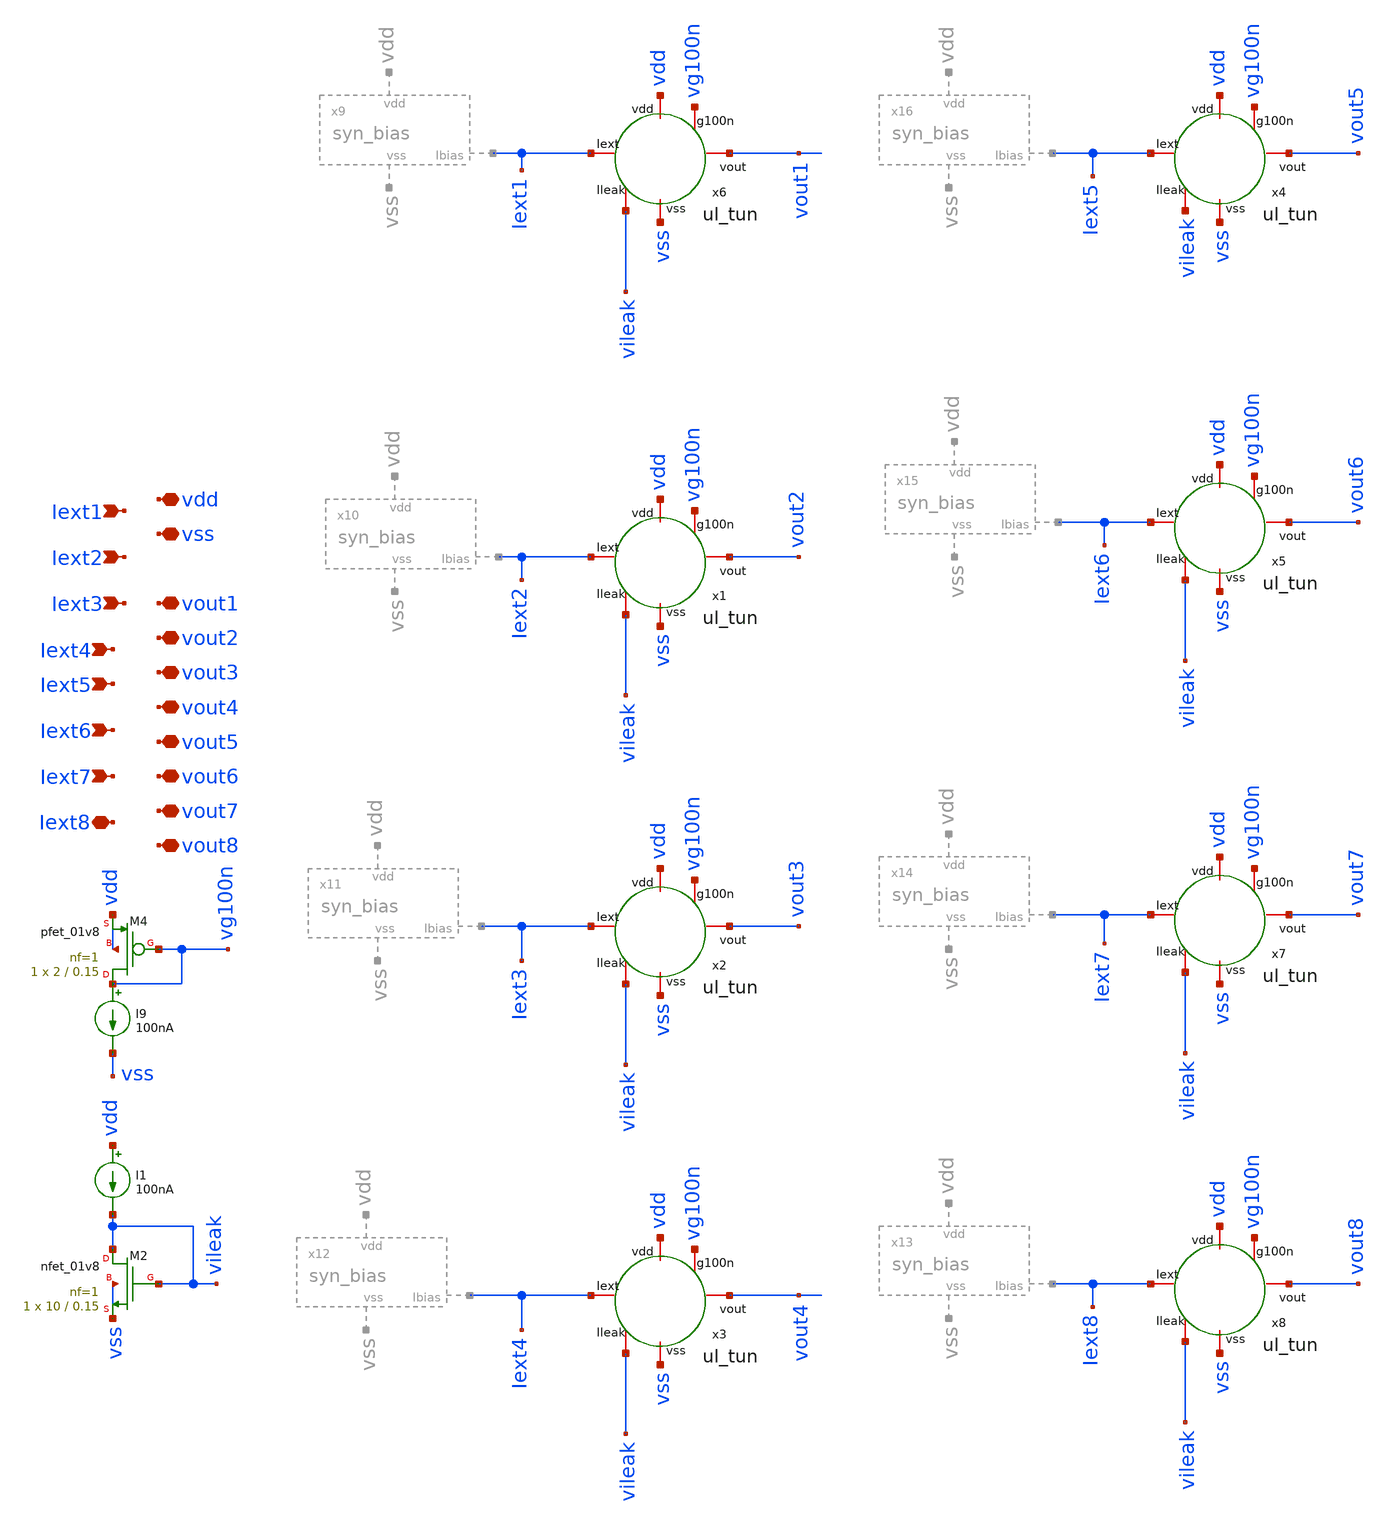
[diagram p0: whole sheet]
** sch_path: layer/layer_hidden.sch
**.subckt layer_hidden vdd vss Iext1 Iext2 Iext3 Iext4 vout1 vout2 vout3 vout4 Iext5 Iext6 Iext7
*+ Iext8 vout5 vout6 vout7 vout8
*.iopin vdd
*.iopin vss
*.ipin Iext1
*.ipin Iext2
*.ipin Iext3
*.ipin Iext4
*.iopin vout1
*.iopin vout2
*.iopin vout3
*.iopin vout4
*.ipin Iext5
*.ipin Iext6
*.ipin Iext7
*.iopin Iext8
*.iopin vout5
*.iopin vout6
*.iopin vout7
*.iopin vout8
x6 Iext1 vdd vg100n vout1 vileak vss ul_tun
I9 vg100n vss 100nA
XM4 vg100n vg100n vdd vdd sky130_fd_pr__pfet_01v8 L=0.15 W=2 nf=1 ad='int((nf+1)/2) * W/nf * 0.29' as='int((nf+2)/2) * W/nf * 0.29'
+ pd='2*int((nf+1)/2) * (W/nf + 0.29)' ps='2*int((nf+2)/2) * (W/nf + 0.29)' nrd='0.29 / W' nrs='0.29 / W'
+ sa=0 sb=0 sd=0 mult=1 m=1
XM2 vileak vileak vss vss sky130_fd_pr__nfet_01v8 L=0.15 W=10 nf=1 ad='int((nf+1)/2) * W/nf * 0.29' as='int((nf+2)/2) * W/nf * 0.29'
+ pd='2*int((nf+1)/2) * (W/nf + 0.29)' ps='2*int((nf+2)/2) * (W/nf + 0.29)' nrd='0.29 / W' nrs='0.29 / W'
+ sa=0 sb=0 sd=0 mult=1 m=1
I1 vdd vileak 100nA
x1 Iext2 vdd vg100n vout2 vileak vss ul_tun
x2 Iext3 vdd vg100n vout3 vileak vss ul_tun
x3 Iext4 vdd vg100n vout4 vileak vss ul_tun
x8 Iext8 vdd vg100n vout8 vileak vss ul_tun
x4 Iext5 vdd vg100n vout5 vileak vss ul_tun
x5 Iext6 vdd vg100n vout6 vileak vss ul_tun
x7 Iext7 vdd vg100n vout7 vileak vss ul_tun
**.ends

* expanding   symbol:  Neuron/ultralif/ul_tun.sym # of pins=6
** sym_path: Neuron/ultralif/ul_tun.sym
** sch_path: Neuron/ultralif/ul_tun.sch
.subckt ul_tun Iext vdd g100n vout Ileak vss
*.iopin Iext
*.iopin vout
*.iopin vss
*.iopin Ileak
*.iopin vdd
*.iopin g100n
XM1 Ileak Ileak net1 vdd sky130_fd_pr__pfet_01v8 L=10 W=1 nf=1 ad='int((nf+1)/2) * W/nf * 0.29' as='int((nf+2)/2) * W/nf * 0.29'
+ pd='2*int((nf+1)/2) * (W/nf + 0.29)' ps='2*int((nf+2)/2) * (W/nf + 0.29)' nrd='0.29 / W' nrs='0.29 / W'
+ sa=0 sb=0 sd=0 mult=1 m=1
XM2 Ileak net2 net1 vdd sky130_fd_pr__pfet_01v8 L=0.15 W=1.5 nf=1 ad='int((nf+1)/2) * W/nf * 0.29' as='int((nf+2)/2) * W/nf * 0.29'
+ pd='2*int((nf+1)/2) * (W/nf + 0.29)' ps='2*int((nf+2)/2) * (W/nf + 0.29)' nrd='0.29 / W' nrs='0.29 / W'
+ sa=0 sb=0 sd=0 mult=1 m=1
XM3 net2 net2 net1 vdd sky130_fd_pr__pfet_01v8 L=0.15 W=15 nf=1 ad='int((nf+1)/2) * W/nf * 0.29' as='int((nf+2)/2) * W/nf * 0.29'
+ pd='2*int((nf+1)/2) * (W/nf + 0.29)' ps='2*int((nf+2)/2) * (W/nf + 0.29)' nrd='0.29 / W' nrs='0.29 / W'
+ sa=0 sb=0 sd=0 mult=1 m=1
XM4 net2 Ileak vss vss sky130_fd_pr__nfet_01v8 L=4 W=1 nf=1 ad='int((1 + 1)/2) * 1 / 1 * 0.29' as='int((1 + 2)/2) * 1 / 1 * 0.29'
+ pd='2*int((1 + 1)/2) * (1 / 1 + 0.29)' ps='2*int((1 + 2)/2) * (1 / 1 + 0.29)' nrd='0.29 / 1 ' nrs='0.29 / 1 '
+ sa=0 sb=0 sd=0 mult=1 m=1
C1 net1 vss 1p m=1
XM5 vout_n Ileak vss vss sky130_fd_pr__nfet_01v8 L=0.15 W=1 nf=1 ad='int((1 + 1)/2) * 1 / 1 * 0.29' as='int((1 + 2)/2) * 1 / 1 * 0.29'
+ pd='2*int((1 + 1)/2) * (1 / 1 + 0.29)' ps='2*int((1 + 2)/2) * (1 / 1 + 0.29)' nrd='0.29 / 1 ' nrs='0.29 / 1 '
+ sa=0 sb=0 sd=0 mult=1 m=1
XM6 vout_n g100n vdd vdd sky130_fd_pr__pfet_01v8 L=0.15 W=2 nf=1 ad='int((nf+1)/2) * W/nf * 0.29' as='int((nf+2)/2) * W/nf * 0.29'
+ pd='2*int((nf+1)/2) * (W/nf + 0.29)' ps='2*int((nf+2)/2) * (W/nf + 0.29)' nrd='0.29 / W' nrs='0.29 / W'
+ sa=0 sb=0 sd=0 mult=1 m=1
XM7 vout vout_n vss vss sky130_fd_pr__nfet_01v8 L=0.15 W=1 nf=1 ad='int((1 + 1)/2) * 1 / 1 * 0.29' as='int((1 + 2)/2) * 1 / 1 * 0.29'
+ pd='2*int((1 + 1)/2) * (1 / 1 + 0.29)' ps='2*int((1 + 2)/2) * (1 / 1 + 0.29)' nrd='0.29 / 1 ' nrs='0.29 / 1 '
+ sa=0 sb=0 sd=0 mult=1 m=1
XM8 vout vout_n vdd vdd sky130_fd_pr__pfet_01v8 L=0.15 W=2 nf=1 ad='int((nf+1)/2) * W/nf * 0.29' as='int((nf+2)/2) * W/nf * 0.29'
+ pd='2*int((nf+1)/2) * (W/nf + 0.29)' ps='2*int((nf+2)/2) * (W/nf + 0.29)' nrd='0.29 / W' nrs='0.29 / W'
+ sa=0 sb=0 sd=0 mult=1 m=1
vext Iext net1 0
**** begin user architecture code


.save i(vext)


**** end user architecture code
.ends


* expanding   symbol:  /foss/designs/SNN_IPN/Neuron/ultralif/syn_bias.sym # of pins=3
** sym_path: Neuron/ultralif/syn_bias.sym
** sch_path: Neuron/ultralif/syn_bias.sch
.subckt syn_bias vdd vss Ibias
*.iopin vss
*.iopin vdd
*.iopin Ibias
XM2 Ibias net1 vdd vdd sky130_fd_pr__pfet_01v8 L=1 W=0.5 nf=1 ad='int((nf+1)/2) * W/nf * 0.29' as='int((nf+2)/2) * W/nf * 0.29'
+ pd='2*int((nf+1)/2) * (W/nf + 0.29)' ps='2*int((nf+2)/2) * (W/nf + 0.29)' nrd='0.29 / W' nrs='0.29 / W'
+ sa=0 sb=0 sd=0 mult=1 m=1
XR1 net1 vdd sky130_fd_pr__res_generic_po W=1.15 L=1 m=1
XR2 vss net1 sky130_fd_pr__res_generic_po W=1 L=1 m=1
.ends

.end
